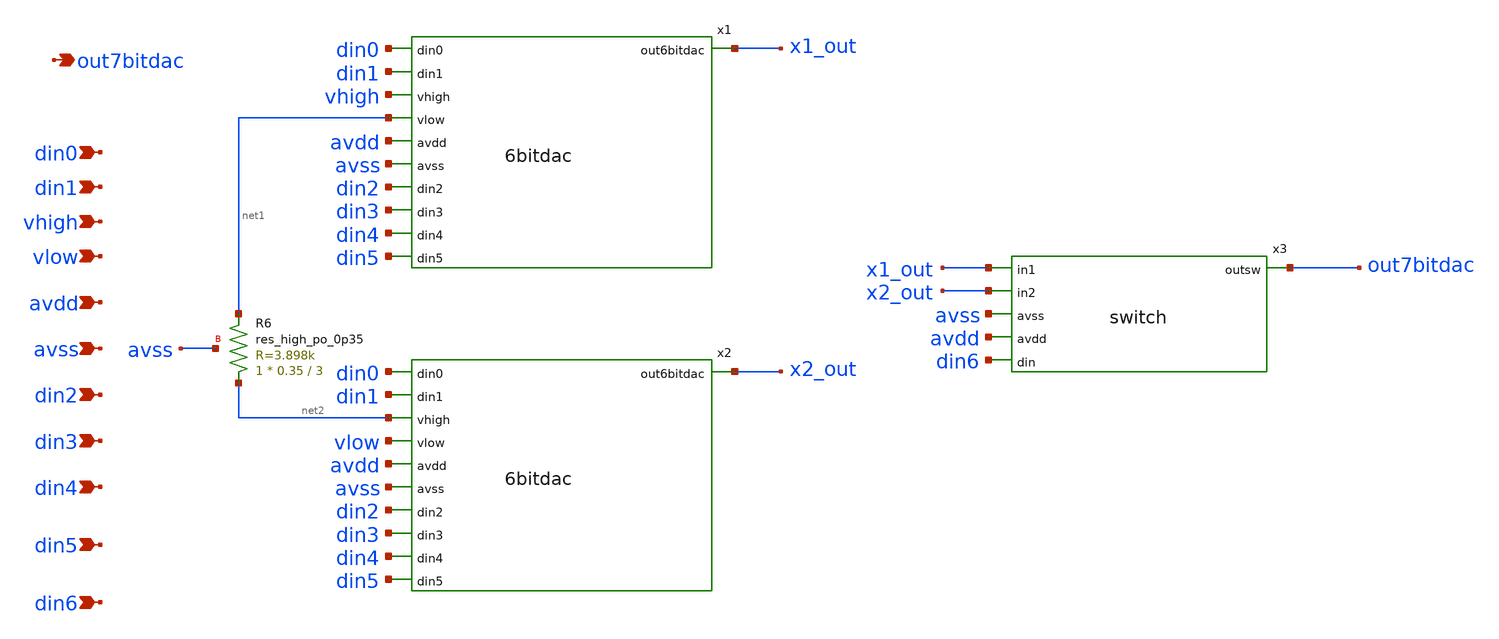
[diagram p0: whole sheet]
** sch_path: xschem/7bitdac.sch
**.subckt 7bitdac din0 din1 vhigh vlow avdd avss din2 din3 out7bitdac din4 din5 din6
*.ipin din0
*.ipin din1
*.ipin vhigh
*.ipin vlow
*.ipin avdd
*.ipin avss
*.ipin din2
*.ipin din3
*.opin out7bitdac
*.ipin din4
*.ipin din5
*.ipin din6
x1 x1_out din0 din1 vhigh net1 avdd avss din2 din3 din4 din5 6bitdac
x2 x2_out din0 din1 net2 vlow avdd avss din2 din3 din4 din5 6bitdac
x3 out7bitdac x1_out x2_out avss avdd din6 switch
XR6 net2 net1 avss sky130_fd_pr__res_high_po_0p35 L=3 mult=1 m=1
**.ends
.end
